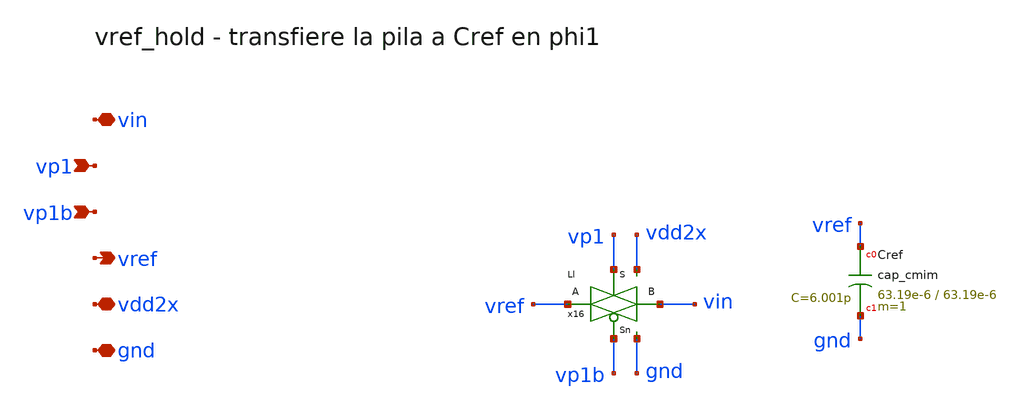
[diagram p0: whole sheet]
** sch_path: Enfoque_A/xschem/celdas/vref_hold.sch
**.subckt vref_hold vin vp1 vp1b vref vdd2x gnd
*.iopin vin
*.ipin vp1
*.ipin vp1b
*.opin vref
*.iopin vdd2x
*.iopin gnd
x16 vref vin vp1 vp1b vdd2x gnd Ll
XCref vref gnd cap_cmim w=63.19e-6 l=63.19e-6 m=1 mm_ok=1
**.ends

* expanding   symbol:  Enfoque_A/xschem/celdas/Ll.sym # of pins=6
** sym_path: Enfoque_A/xschem/celdas/Ll.sym
** sch_path: Enfoque_A/xschem/celdas/Ll.sch
.subckt Ll A B S Sn vdd gnd
*.iopin gnd
*.iopin vdd
*.iopin B
*.ipin Sn
*.ipin S
*.iopin A
XM101 A S B gnd sg13_lv_nmos w=0.13u l=0.130u ng=1 m=1 mm_ok=1
XM100 B Sn A vdd sg13_lv_pmos w=0.3u l=0.130u ng=1 m=1 mm_ok=1
.ends

.end
